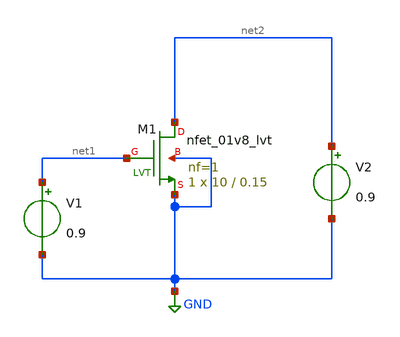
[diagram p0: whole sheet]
** sch_path: MOS-Design-Parameters/act6.sch
**.subckt act6
XM1 net2 net1 GND GND sky130_fd_pr__nfet_01v8_lvt L=0.15 W=10 nf=1 ad='int((nf+1)/2) * W/nf * 0.29' as='int((nf+2)/2) * W/nf * 0.29'
+ pd='2*int((nf+1)/2) * (W/nf + 0.29)' ps='2*int((nf+2)/2) * (W/nf + 0.29)' nrd='0.29 / W' nrs='0.29 / W'
+ sa=0 sb=0 sd=0 mult=1 m=1
V1 net1 GND 0.9
V2 net2 GND 0.9
**** begin user architecture code


.lib /usr/local/share/pdk/sky130A/libs.tech/ngspice/sky130.lib.spice ff
.option wnflag=1 scale=1e-6

.control
save all

save @m.xm1.msky130_fd_pr__nfet_01v8_lvt[id]
save @m.xm1.msky130_fd_pr__nfet_01v8_lvt[gm]

dc v1 0 1.8 1m

let id = @m.xm1.msky130_fd_pr__nfet_01v8_lvt[id]
let gm = @m.xm1.msky130_fd_pr__nfet_01v8_lvt[gm]
let gmoverid = gm/id

wrdata id-ff.txt id
wrdata gm-ff.txt gm
wrdata gmoverid-ff.txt gmoverid

.endc


**** end user architecture code
**.ends
.GLOBAL GND
.end
